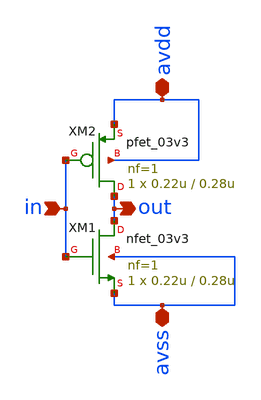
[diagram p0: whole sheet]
** sch_path: designs/libs/snn_analog/stdp/sch/stdp/not.sch
**.subckt not avdd avss in out
*.iopin avdd
*.iopin avss
*.ipin in
*.opin out
XM1 out in avss avss nfet_03v3 L=0.28u W=0.22u nf=1 ad='int((nf+1)/2) * W/nf * 0.18u' as='int((nf+2)/2) * W/nf * 0.18u'
+ pd='2*int((nf+1)/2) * (W/nf + 0.18u)' ps='2*int((nf+2)/2) * (W/nf + 0.18u)' nrd='0.18u / W' nrs='0.18u / W'
+ sa=0 sb=0 sd=0 m=1
XM2 out in avdd avdd pfet_03v3 L=0.28u W=0.22u nf=1 ad='int((nf+1)/2) * W/nf * 0.18u' as='int((nf+2)/2) * W/nf * 0.18u'
+ pd='2*int((nf+1)/2) * (W/nf + 0.18u)' ps='2*int((nf+2)/2) * (W/nf + 0.18u)' nrd='0.18u / W' nrs='0.18u / W'
+ sa=0 sb=0 sd=0 m=1
**.ends
.end
